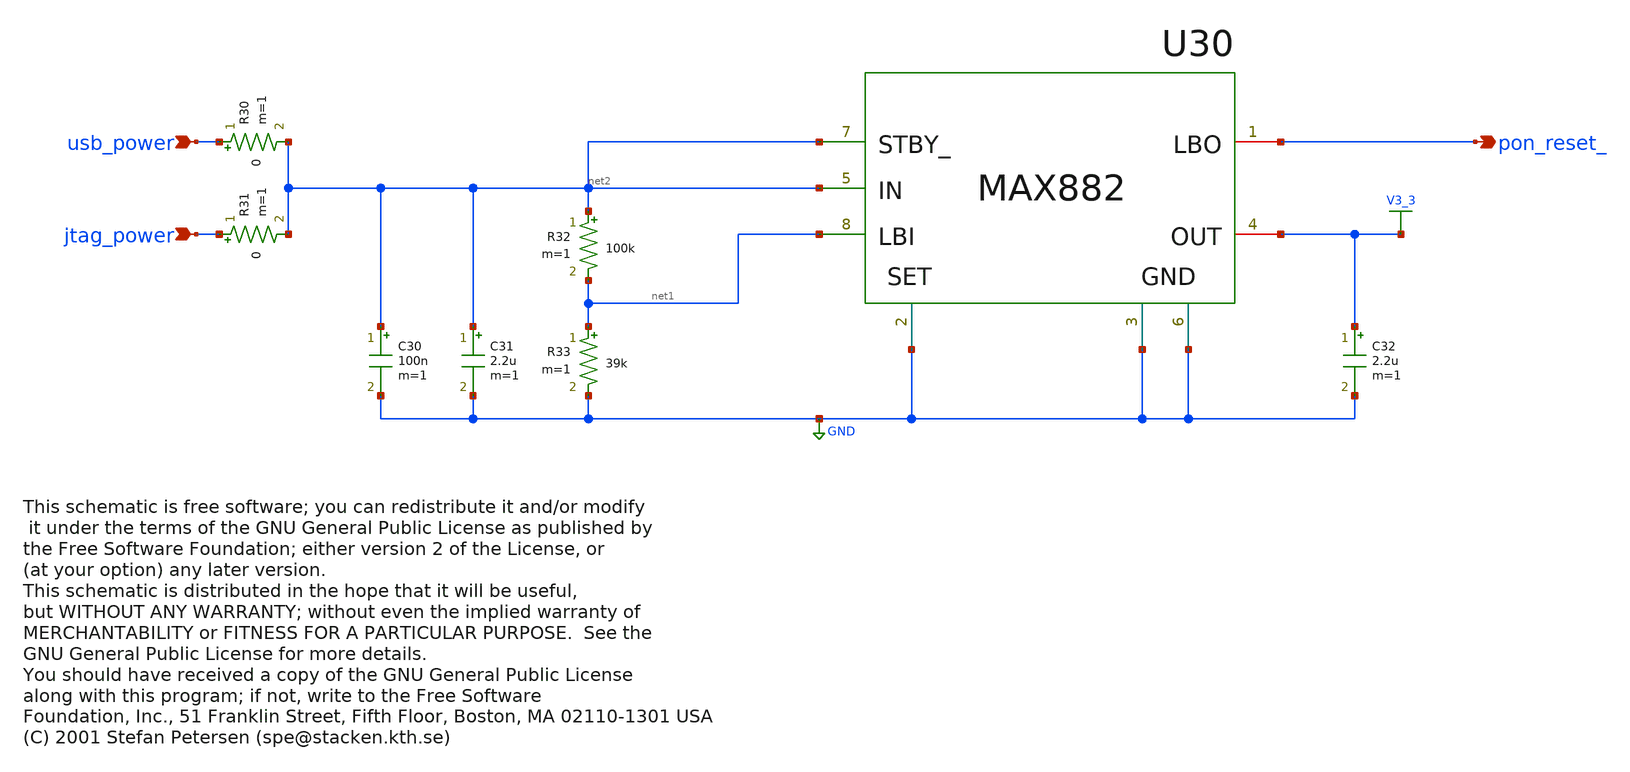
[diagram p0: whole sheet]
** sch_path: xschem_libraries_oa/xTAG/xTAG-psu/schematic/xTAG-psu.sch
* Copyright (C) 1998-2024 Stefan Frederik Schippers
* This program is free software; you can redistribute it and/or modify
* it under the terms of the GNU General Public License as published by
* the Free Software Foundation; either version 2 of the License, or
* (at your option) any later version.
* This program is distributed in the hope that it will be useful,
* but WITHOUT ANY WARRANTY; without even the implied warranty of
* MERCHANTABILITY or FITNESS FOR A PARTICULAR PURPOSE.  See the
* GNU General Public License for more details.
* You should have received a copy of the GNU General Public License
* along with this program; if not, write to the Free Software
* This schematic is free software; you can redistribute it and/or modify
* (C) 2001 Stefan Petersen (spe@stacken.kth.se)
**.subckt xTAG-psu usb_power jtag_power pon_reset_
*.ipin usb_power
*.ipin jtag_power
*.opin pon_reset_
U30 net2 net2 net1 pon_reset_ V3_3 GND GND max882
R32 net2 net1 100k m=1
R33 net1 GND 39k m=1
C31 net2 GND 2.2u m=1
C30 net2 GND 100n m=1
R30 usb_power net2 0 m=1
R31 jtag_power net2 0 m=1
C32 V3_3 GND 2.2u m=1
**.ends
.GLOBAL V3_3
.GLOBAL GND
.end
